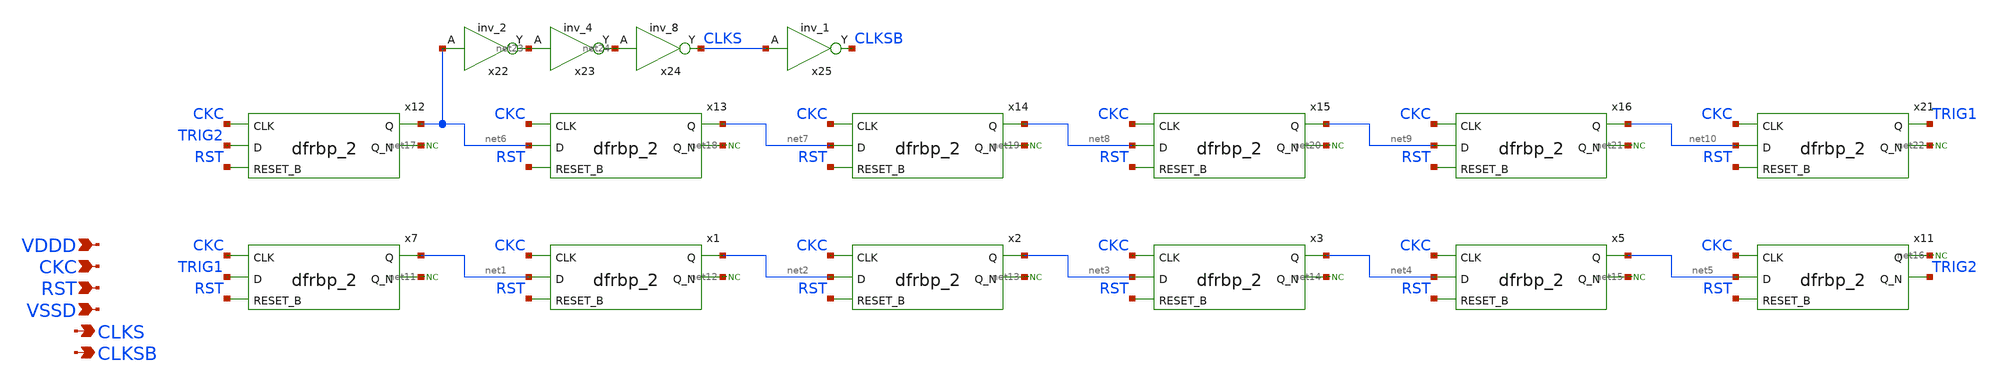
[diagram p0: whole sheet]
** sch_path: xschem/auto_sampling.sch
**.subckt auto_sampling CKC VDDD VSSD CLKS CLKSB RST
*.ipin CKC
*.ipin VDDD
*.ipin VSSD
*.opin CLKS
*.opin CLKSB
*.ipin RST
x7 CKC TRIG1 RST VSSD VSSD VDDD VDDD net1 net11 sky130_fd_sc_hd__dfrbp_2
x1 CKC net1 RST VSSD VSSD VDDD VDDD net2 net12 sky130_fd_sc_hd__dfrbp_2
x2 CKC net2 RST VSSD VSSD VDDD VDDD net3 net13 sky130_fd_sc_hd__dfrbp_2
x3 CKC net3 RST VSSD VSSD VDDD VDDD net4 net14 sky130_fd_sc_hd__dfrbp_2
* noconn #net11
* noconn #net12
* noconn #net13
x5 CKC net4 RST VSSD VSSD VDDD VDDD net5 net15 sky130_fd_sc_hd__dfrbp_2
* noconn #net14
x11 CKC net5 RST VSSD VSSD VDDD VDDD net16 TRIG2 sky130_fd_sc_hd__dfrbp_2
* noconn #net16
* noconn #net15
x12 CKC TRIG2 RST VSSD VSSD VDDD VDDD net6 net17 sky130_fd_sc_hd__dfrbp_2
x13 CKC net6 RST VSSD VSSD VDDD VDDD net7 net18 sky130_fd_sc_hd__dfrbp_2
x14 CKC net7 RST VSSD VSSD VDDD VDDD net8 net19 sky130_fd_sc_hd__dfrbp_2
x15 CKC net8 RST VSSD VSSD VDDD VDDD net9 net20 sky130_fd_sc_hd__dfrbp_2
* noconn #net17
* noconn #net18
* noconn #net19
x16 CKC net9 RST VSSD VSSD VDDD VDDD net10 net21 sky130_fd_sc_hd__dfrbp_2
* noconn #net20
x21 CKC net10 RST VSSD VSSD VDDD VDDD TRIG1 net22 sky130_fd_sc_hd__dfrbp_2
* noconn #net22
* noconn #net21
x22 net6 VSSD VSSD VDDD VDDD net23 sky130_fd_sc_hd__inv_2
x23 net23 VSSD VSSD VDDD VDDD net24 sky130_fd_sc_hd__inv_4
x24 net24 VSSD VSSD VDDD VDDD CLKS sky130_fd_sc_hd__inv_8
x25 CLKS VSSD VSSD VDDD VDDD CLKSB sky130_fd_sc_hd__inv_1
**.ends
.end
